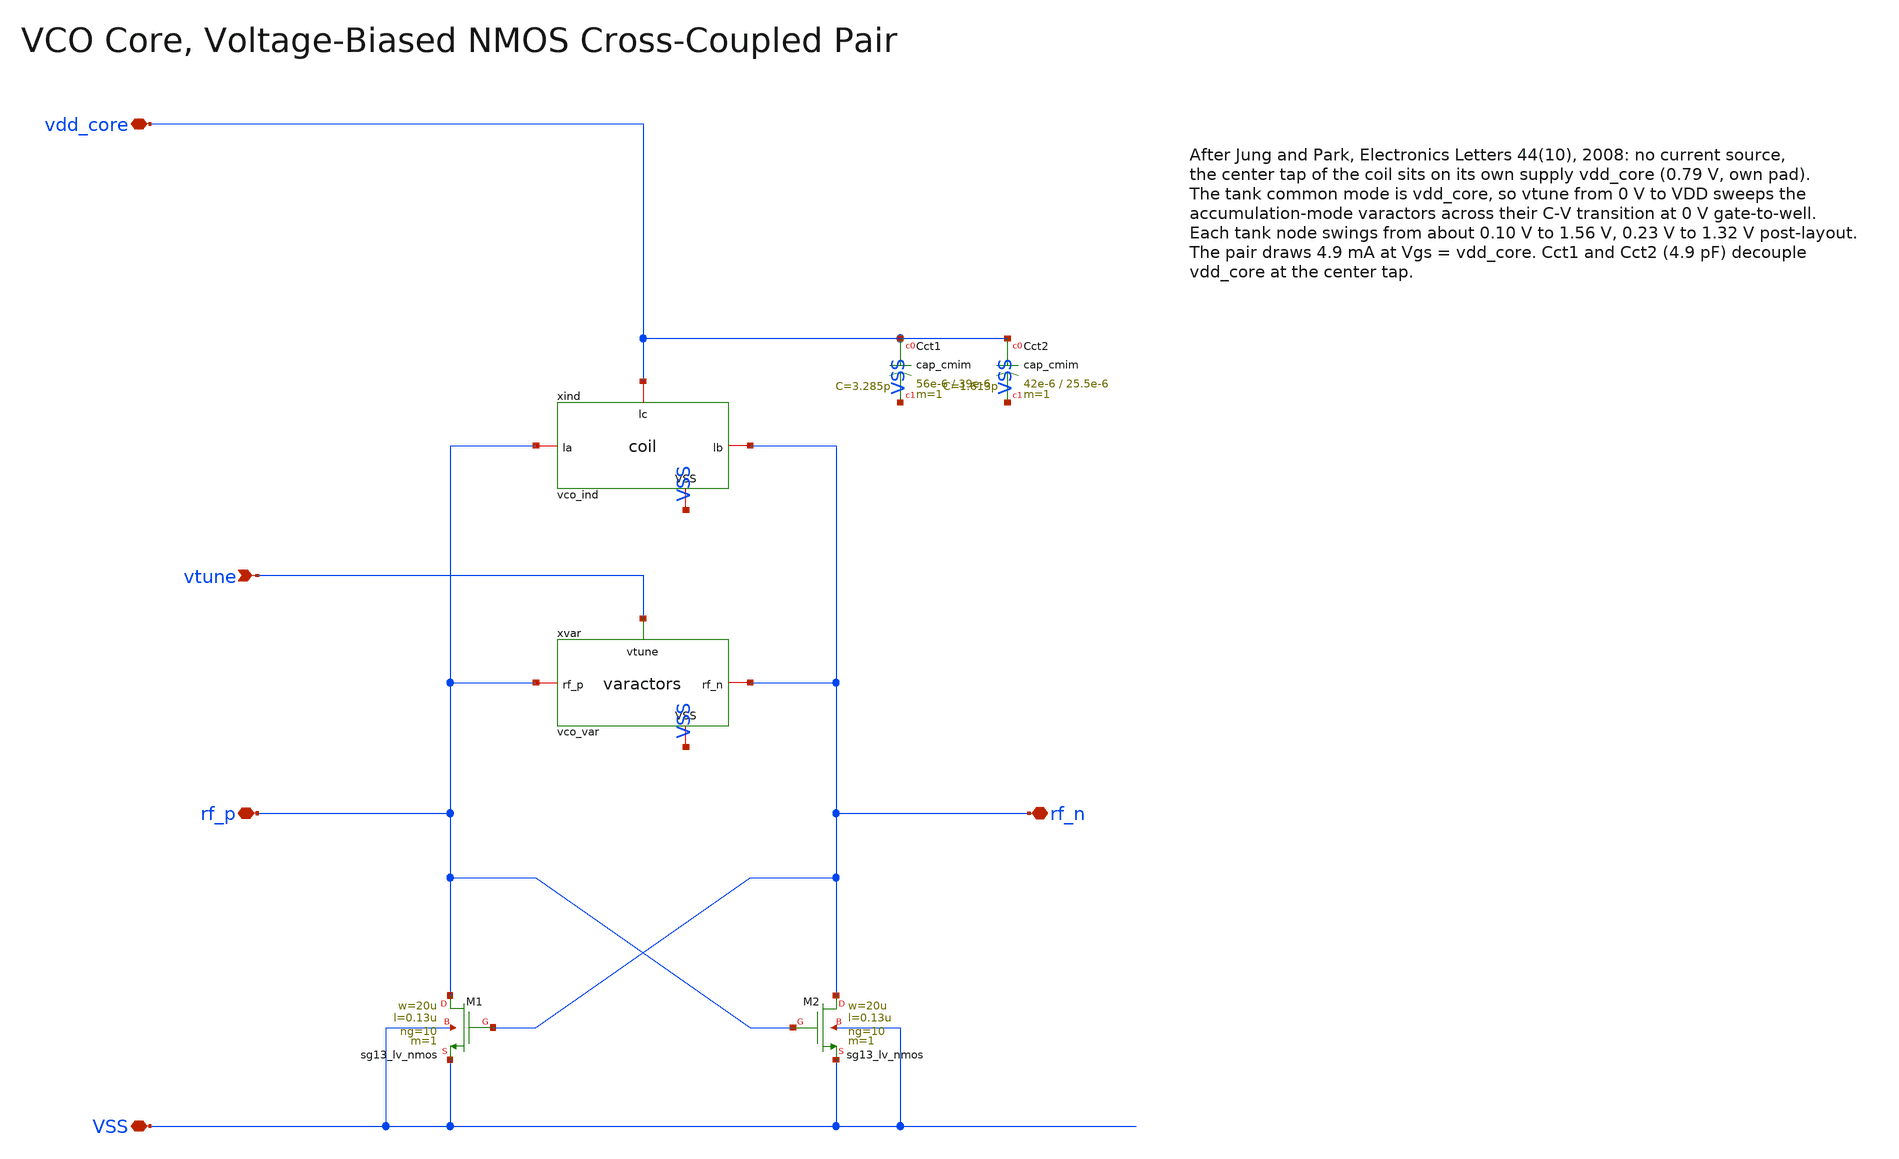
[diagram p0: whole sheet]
** sch_path: macros/vco/schematic/xschem/vco_core.sch
**.subckt vco_core vdd_core VSS vtune rf_p rf_n
*.iopin vdd_core
*.iopin VSS
*.ipin vtune
*.iopin rf_p
*.iopin rf_n
xind rf_p rf_n vdd_core VSS vco_ind
XCct1 vdd_core VSS cap_cmim w=56e-6 l=39e-6 m=1 mm_ok=1
xvar rf_p rf_n vtune VSS vco_var
XM1 rf_p rf_n VSS VSS sg13_lv_nmos w=20u l=0.13u ng=10 m=1 mm_ok=1
XM2 rf_n rf_p VSS VSS sg13_lv_nmos w=20u l=0.13u ng=10 m=1 mm_ok=1
XCct2 vdd_core VSS cap_cmim w=42e-6 l=25.5e-6 m=1 mm_ok=1
**.ends

* expanding   symbol:  vco_ind.sym # of pins=4
** sym_path: macros/vco/schematic/xschem/vco_ind.sym
** sch_path: macros/vco/schematic/xschem/vco_ind.sch
.subckt vco_ind la lb lc VSS
*.iopin la
*.iopin lc
*.iopin lb
*.iopin VSS
XL1 la lc lb VSS inductor3 w=4e-6 s=4e-6 d=52e-6 nr_r=2 m=1
x1 la lb lc vco_ind_le
.ends


* expanding   symbol:  vco_var.sym # of pins=4
** sym_path: macros/vco/schematic/xschem/vco_var.sym
** sch_path: macros/vco/schematic/xschem/vco_var.sch
.subckt vco_var rf_p rf_n vtune VSS
*.ipin vtune
*.iopin rf_p
*.iopin rf_n
*.iopin VSS
XCvar1 rf_p vtune rf_n VSS sg13_hv_svaricap w=3.74u l=0.3u Nx=7 mm_ok=1
XCvar2 rf_p vtune rf_n VSS sg13_hv_svaricap w=3.74u l=0.3u Nx=7 mm_ok=1
XCvar3 rf_p vtune rf_n VSS sg13_hv_svaricap w=3.74u l=0.3u Nx=7 mm_ok=1
.ends

.end
